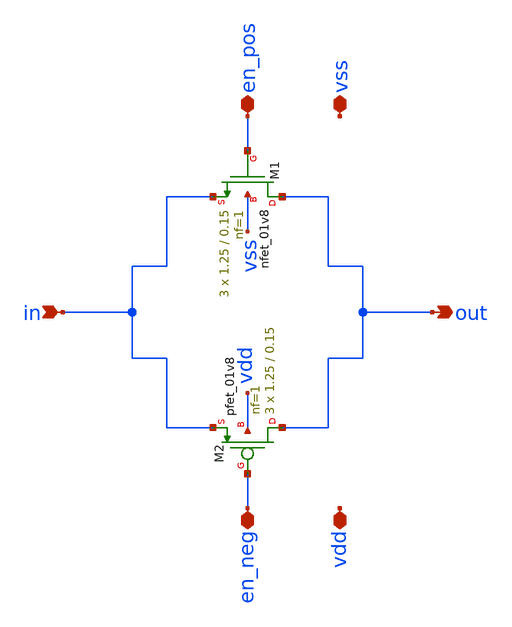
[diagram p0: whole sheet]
** sch_path: xschem/trans_gate_mux2to8.sch
**.subckt trans_gate_mux2to8 en_neg in out en_pos vdd vss
*.iopin en_neg
*.ipin in
*.opin out
*.iopin en_pos
*.iopin vdd
*.iopin vss
XM2 out en_neg in vdd sky130_fd_pr__pfet_01v8 L=0.15 W=1.25 nf=1 ad='int((nf+1)/2) * W/nf * 0.29' as='int((nf+2)/2) * W/nf * 0.29'
+ pd='2*int((nf+1)/2) * (W/nf + 0.29)' ps='2*int((nf+2)/2) * (W/nf + 0.29)' nrd='0.29 / W' nrs='0.29 / W'
+ sa=0 sb=0 sd=0 mult=3 m=3
XM1 out en_pos in vss sky130_fd_pr__nfet_01v8 L=0.15 W=1.25 nf=1 ad='int((nf+1)/2) * W/nf * 0.29' as='int((nf+2)/2) * W/nf * 0.29'
+ pd='2*int((nf+1)/2) * (W/nf + 0.29)' ps='2*int((nf+2)/2) * (W/nf + 0.29)' nrd='0.29 / W' nrs='0.29 / W'
+ sa=0 sb=0 sd=0 mult=3 m=3
**.ends
.end
